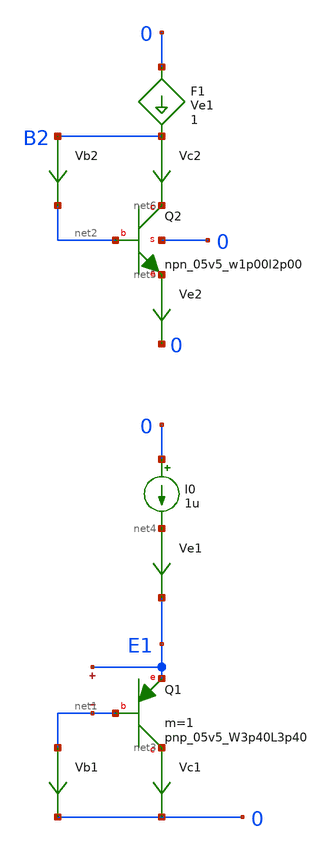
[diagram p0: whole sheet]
** sch_path: sky130A/xschem_libs/sky130_tests_ase/test_bipolar/schematic/test_bipolar.sch
* Copyright 2021 Stefan Frederik Schippers
* Licensed under the Apache License, Version 2.0 (the "License");
* you may not use this file except in compliance with the License.
* You may obtain a copy of the License at
* https://www.apache.org/licenses/LICENSE-2.0
* Unless required by applicable law or agreed to in writing, software
* distributed under the License is distributed on an "AS IS" BASIS,
* WITHOUT WARRANTIES OR CONDITIONS OF ANY KIND, either express or implied.
* See the License for the specific language governing permissions and
* limitations under the License.
**.subckt test_bipolar
XQ1 net3 net1 E1 sky130_fd_pr__pnp_05v5_W3p40L3p40 m=1
Vc1 net3 0 0
.save i(vc1)
Vb1 net1 0 0
.save i(vb1)
I0 0 net4 1u
Ve1 net4 E1 0
.save i(ve1)
.save v(e1)
.save v(net1)
Ve2 net5 0 0
.save i(ve2)
Vc2 B2 net6 0
.save i(vc2)
Vb2 B2 net2 0
.save i(vb2)
XQ2 net6 net2 net5 0 sky130_fd_pr__npn_05v5_w1p00l2p00
F1 0 B2 Ve1 1
**.ends
.end
